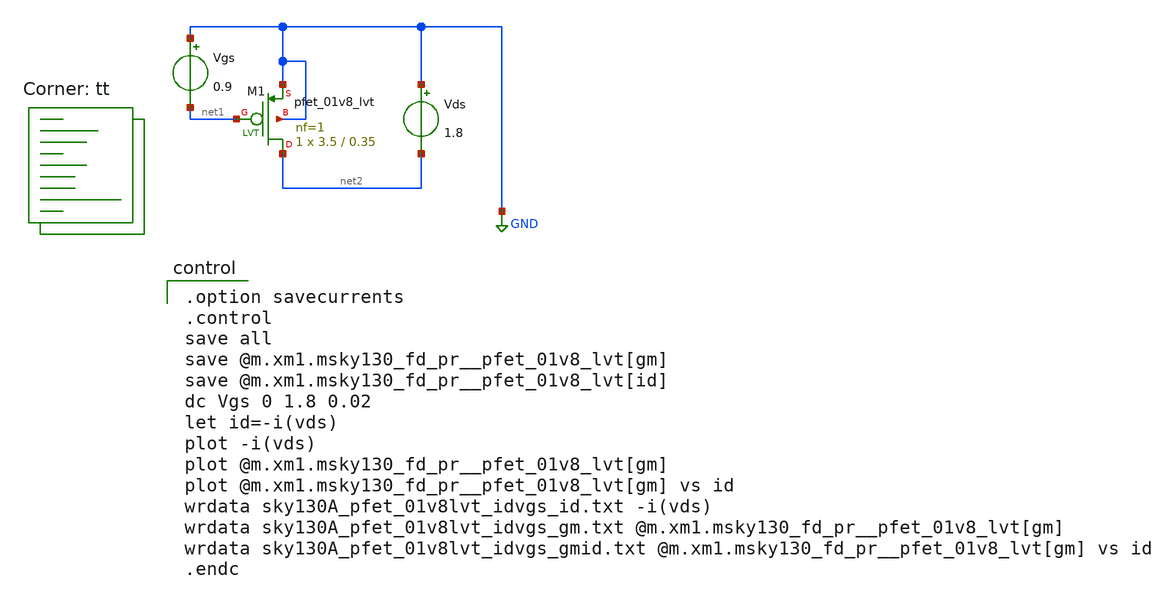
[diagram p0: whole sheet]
** sch_path: xschem/MOSFET/sky130A_pfet_01v8lvt_idvgs.sch
**.subckt sky130A_pfet_01v8lvt_idvgs
Vgs GND net1 0.9
Vds GND net2 1.8
XM1 net2 net1 GND GND sky130_fd_pr__pfet_01v8_lvt L=0.35 W=3.5 nf=1 ad='int((1 + 1)/2) * 3.5 / 1 * 0.29'
+ as='int((1 + 2)/2) * 3.5 / 1 * 0.29' pd='2*int((1 + 1)/2) * (3.5 / 1 + 0.29)' ps='2*int((1 + 2)/2) * (3.5 / 1 + 0.29)'
+ nrd='0.29 / 3.5 ' nrs='0.29 / 3.5 ' sa=0 sb=0 sd=0 mult=1 m=1
**** begin user architecture code

.option savecurrents
.control
save all
save @m.xm1.msky130_fd_pr__pfet_01v8_lvt[gm]
save @m.xm1.msky130_fd_pr__pfet_01v8_lvt[id]
dc Vgs 0 1.8 0.02
let id=-i(vds)
plot -i(vds)
plot @m.xm1.msky130_fd_pr__pfet_01v8_lvt[gm]
plot @m.xm1.msky130_fd_pr__pfet_01v8_lvt[gm] vs id
wrdata sky130A_pfet_01v8lvt_idvgs_id.txt -i(vds)
wrdata sky130A_pfet_01v8lvt_idvgs_gm.txt @m.xm1.msky130_fd_pr__pfet_01v8_lvt[gm]
wrdata sky130A_pfet_01v8lvt_idvgs_gmid.txt @m.xm1.msky130_fd_pr__pfet_01v8_lvt[gm] vs id
.endc

.lib $::SKYWATER_MODELS/sky130.lib.spice tt
**** end user architecture code
**.ends
.GLOBAL GND
.end
